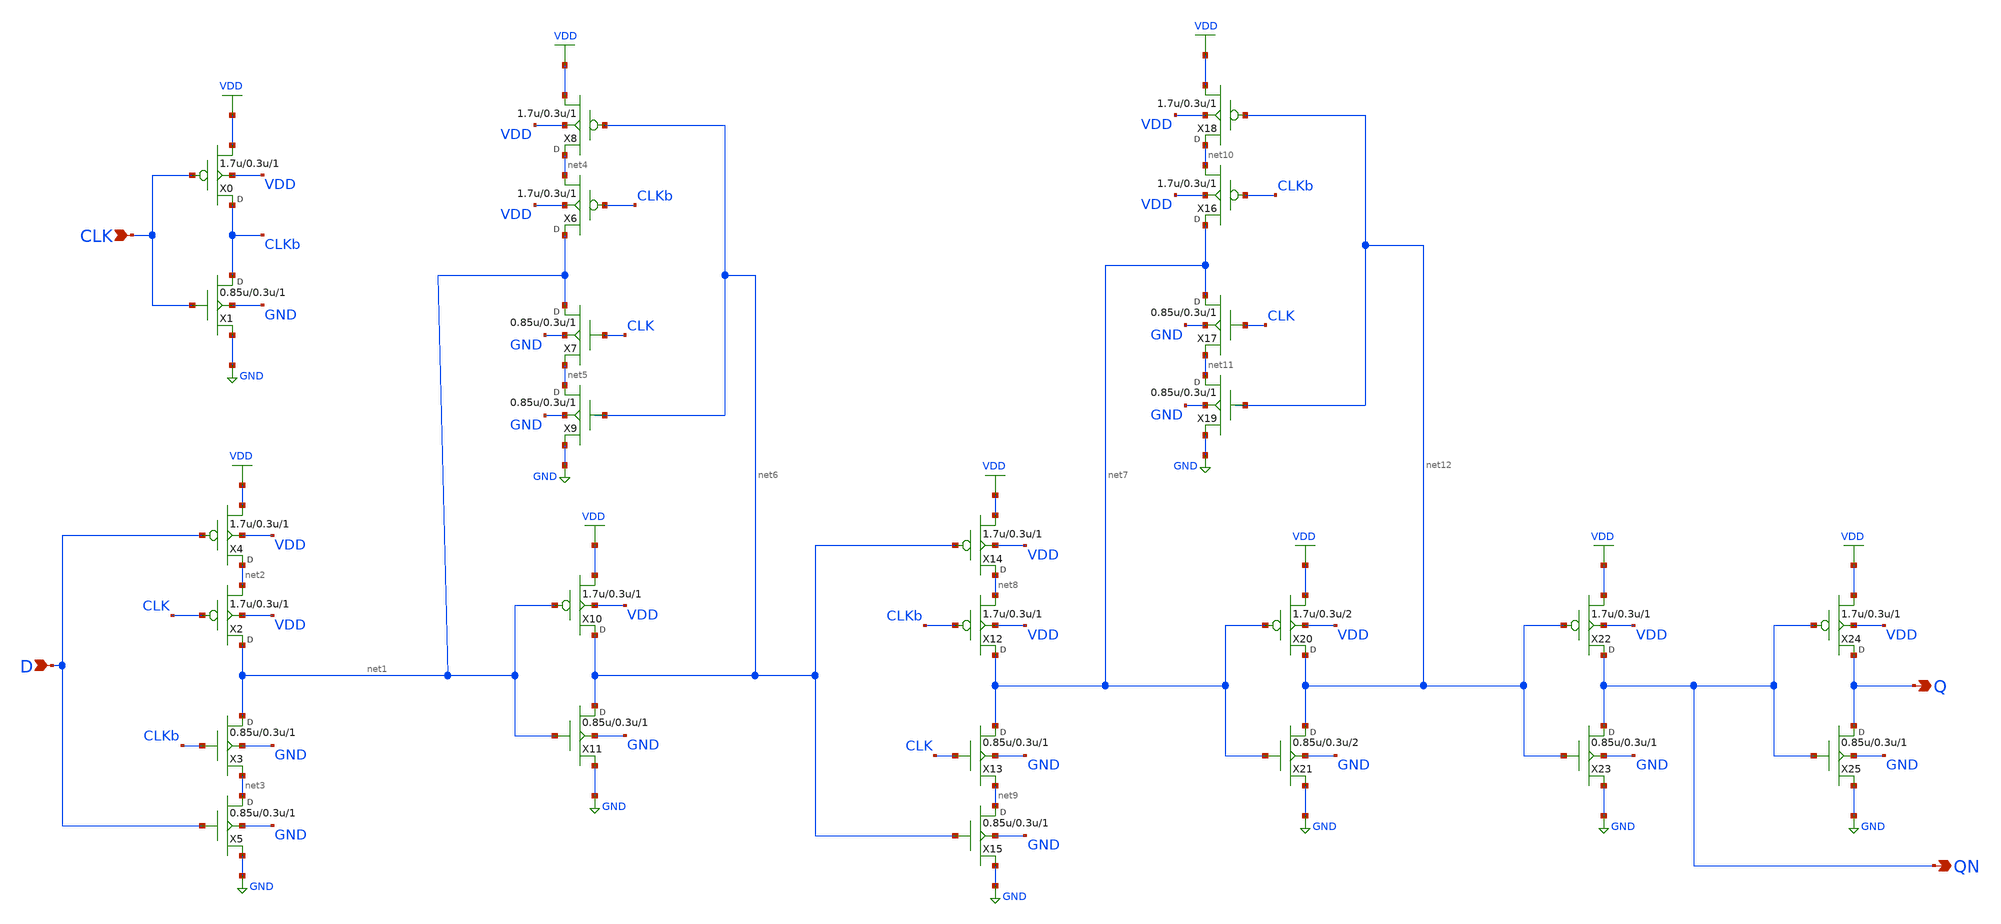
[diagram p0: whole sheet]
** sch_path: gf180mcu_osu_sc_gp9t3v3/cells/dff/gf180mcu_osu_sc_gp9t3v3__dff_1.sch
**.subckt gf180mcu_osu_sc_gp9t3v3__dff_1 CLK D Q QN
*.ipin CLK
*.ipin D
*.opin Q
*.opin QN
X0 CLKb CLK VDD VDD pfet_03p3 w=1.7u l=0.3u m=1
X1 CLKb CLK GND GND nfet_03p3 w=0.85u l=0.3u m=1
X2 net1 CLK net2 VDD pfet_03p3 w=1.7u l=0.3u m=1
X3 net1 CLKb net3 GND nfet_03p3 w=0.85u l=0.3u m=1
X4 net2 D VDD VDD pfet_03p3 w=1.7u l=0.3u m=1
X5 net3 D GND GND nfet_03p3 w=0.85u l=0.3u m=1
X6 net1 CLKb net4 VDD pfet_03p3 w=1.7u l=0.3u m=1
X7 net1 CLK net5 GND nfet_03p3 w=0.85u l=0.3u m=1
X8 net4 net6 VDD VDD pfet_03p3 w=1.7u l=0.3u m=1
X9 net5 net6 GND GND nfet_03p3 w=0.85u l=0.3u m=1
X10 net6 net1 VDD VDD pfet_03p3 w=1.7u l=0.3u m=1
X11 net6 net1 GND GND nfet_03p3 w=0.85u l=0.3u m=1
X12 net7 CLKb net8 VDD pfet_03p3 w=1.7u l=0.3u m=1
X13 net7 CLK net9 GND nfet_03p3 w=0.85u l=0.3u m=1
X14 net8 net6 VDD VDD pfet_03p3 w=1.7u l=0.3u m=1
X15 net9 net6 GND GND nfet_03p3 w=0.85u l=0.3u m=1
X16 net7 CLKb net10 VDD pfet_03p3 w=1.7u l=0.3u m=1
X17 net7 CLK net11 GND nfet_03p3 w=0.85u l=0.3u m=1
X18 net10 net12 VDD VDD pfet_03p3 w=1.7u l=0.3u m=1
X19 net11 net12 GND GND nfet_03p3 w=0.85u l=0.3u m=1
X20 net12 net7 VDD VDD pfet_03p3 w=1.7u l=0.3u m=2
X21 net12 net7 GND GND nfet_03p3 w=0.85u l=0.3u m=2
X22 QN net12 VDD VDD pfet_03p3 w=1.7u l=0.3u m=1
X23 QN net12 GND GND nfet_03p3 w=0.85u l=0.3u m=1
X24 Q QN VDD VDD pfet_03p3 w=1.7u l=0.3u m=1
X25 Q QN GND GND nfet_03p3 w=0.85u l=0.3u m=1
**.ends
.GLOBAL VDD
.GLOBAL GND
.end
